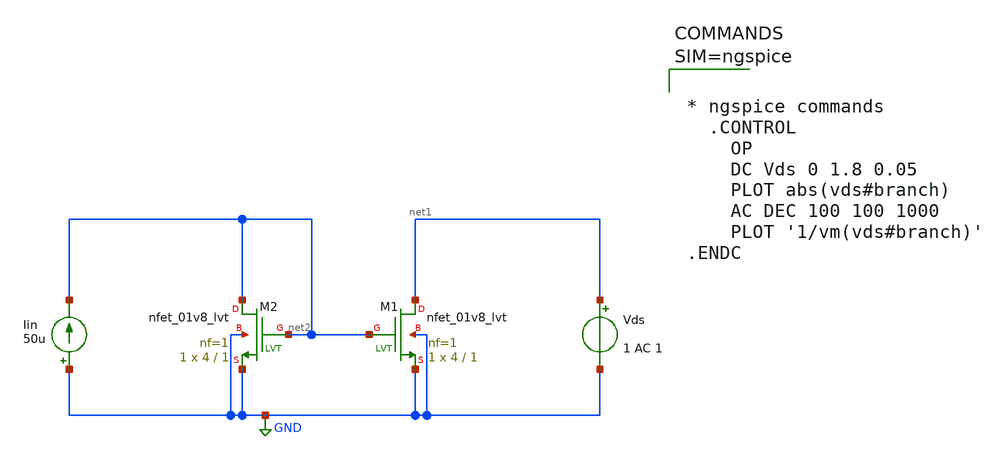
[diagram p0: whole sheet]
** sch_path: xschem/currentmirror.sch
**.subckt currentmirror
Vds net1 GND 1 AC 1
XM1 net1 net2 GND GND sky130_fd_pr__nfet_01v8_lvt L=1 W=4 nf=1 ad='int((1 + 1)/2) * 4 / 1 * 0.29' as='int((1 + 2)/2) * 4 / 1 * 0.29'
+ pd='2*int((1 + 1)/2) * (4 / 1 + 0.29)' ps='2*int((1 + 2)/2) * (4 / 1 + 0.29)' nrd='0.29 / 4 ' nrs='0.29 / 4 '
+ sa=0 sb=0 sd=0 mult=1 m=1
XM2 net2 net2 GND GND sky130_fd_pr__nfet_01v8_lvt L=1 W=4 nf=1 ad='int((1 + 1)/2) * 4 / 1 * 0.29' as='int((1 + 2)/2) * 4 / 1 * 0.29'
+ pd='2*int((1 + 1)/2) * (4 / 1 + 0.29)' ps='2*int((1 + 2)/2) * (4 / 1 + 0.29)' nrd='0.29 / 4 ' nrs='0.29 / 4 '
+ sa=0 sb=0 sd=0 mult=1 m=1
Iin GND net2 50u
**** begin user architecture code

** opencircuitdesign pdks install
.lib $::SKYWATER_MODELS/sky130.lib.spice tt




* ngspice commands
  .CONTROL
    OP
    DC Vds 0 1.8 0.05
    PLOT abs(vds#branch)
    AC DEC 100 100 1000
    PLOT '1/vm(vds#branch)'
.ENDC



**** end user architecture code
**.ends
.GLOBAL GND
.end
